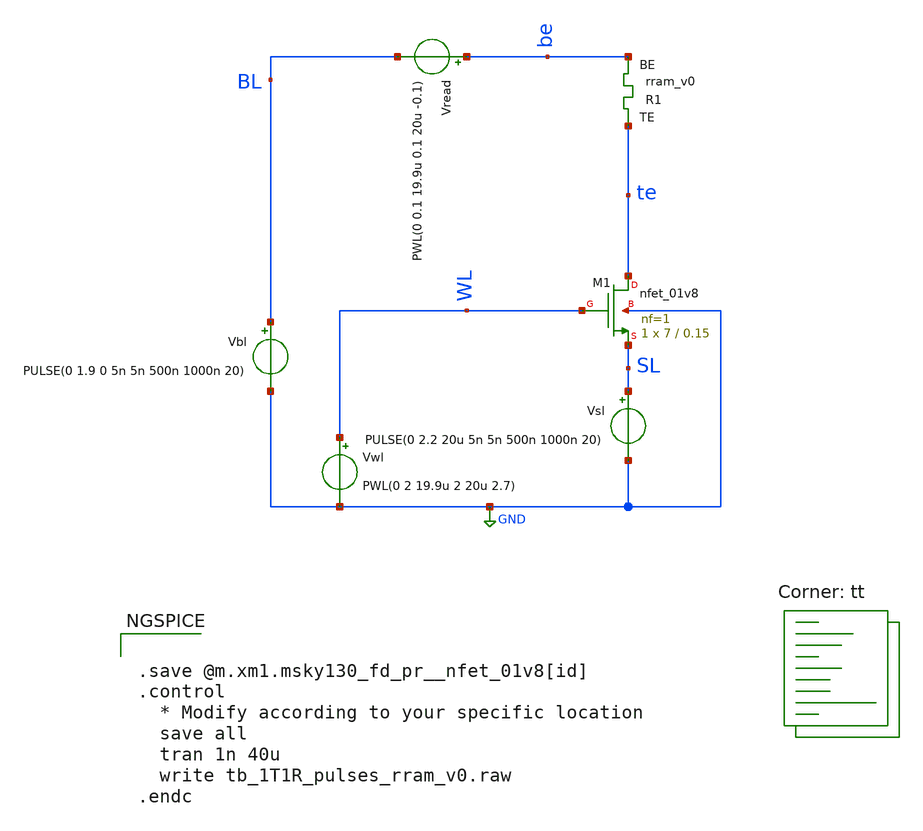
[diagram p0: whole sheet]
** sch_path: memristor_models/wellposed/tb_1T1R_pulses_rram_v0.sch
**.subckt tb_1T1R_pulses_rram_v0
XM1 te WL SL GND sky130_fd_pr__nfet_01v8 L=0.15 W=7 nf=1 ad='int((nf+1)/2) * W/nf * 0.29' as='int((nf+2)/2) * W/nf * 0.29'
+ pd='2*int((nf+1)/2) * (W/nf + 0.29)' ps='2*int((nf+2)/2) * (W/nf + 0.29)' nrd='0.29 / W' nrs='0.29 / W'
+ sa=0 sb=0 sd=0 mult=1 m=1
Vwl WL GND PWL(0 2 19.9u 2 20u 2.7)
Vbl BL GND PULSE(0 1.9 0 5n 5n 500n 1000n 20)
Vread be BL PWL(0 0.1 19.9u 0.1 20u -0.1)
XR1 te be rram_v0
Vsl SL GND PULSE(0 2.2 20u 5n 5n 500n 1000n 20)
**** begin user architecture code


.save @m.xm1.msky130_fd_pr__nfet_01v8[id]
.control
  * Modify according to your specific location
  save all
  tran 1n 40u
  write tb_1T1R_pulses_rram_v0.raw
.endc



.lib $::SKYWATER_MODELS/sky130.lib.spice tt

** opencircuitdesign pdks install
.inc $::SKYWATER_MODELS/rram_v0.spice

**** end user architecture code
**.ends
.GLOBAL GND
.end
